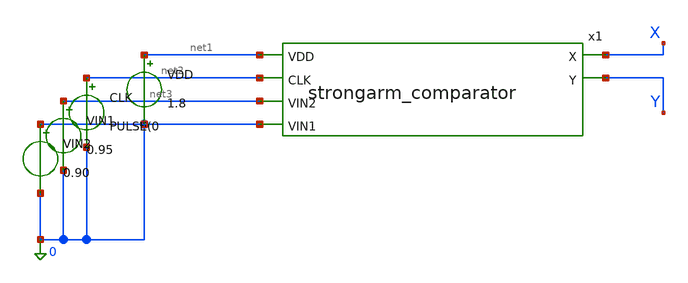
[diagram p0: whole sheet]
** sch_path: strongarm_comparator_tb.sch
**.subckt strongarm_comparator_tb
x1 net1 X Y net2 net3 0 strongarm_comparator
VDD net1 0 1.8
CLK net2 0 PULSE(0
VIN1 net3 0 0.95
VIN2 0 0 0.90
**.ends

* expanding   symbol:  strongarm_comparator.sym # of pins=6
** sym_path: strongarm_comparator.sym
** sch_path: strongarm_comparator.sch
.subckt strongarm_comparator VDD X Y CLK VIN2 VIN1
*.ipin VDD
*.ipin CLK
*.ipin VIN1
*.ipin VIN2
*.opin X
*.opin Y
XS1 P CLK VDD VDD sky130_fd_pr__pfet_01v8 L=0.15 W=1 nf=1 ad='int((nf+1)/2) * W/nf * 0.29' as='int((nf+2)/2) * W/nf * 0.29'
+ pd='2*int((nf+1)/2) * (W/nf + 0.29)' ps='2*int((nf+2)/2) * (W/nf + 0.29)' nrd='0.29 / W' nrs='0.29 / W'
+ sa=0 sb=0 sd=0 mult=1 m=1
XS3 X CLK VDD VDD sky130_fd_pr__pfet_01v8 L=0.15 W=1 nf=1 ad='int((nf+1)/2) * W/nf * 0.29' as='int((nf+2)/2) * W/nf * 0.29'
+ pd='2*int((nf+1)/2) * (W/nf + 0.29)' ps='2*int((nf+2)/2) * (W/nf + 0.29)' nrd='0.29 / W' nrs='0.29 / W'
+ sa=0 sb=0 sd=0 mult=1 m=1
XM5 X Y VDD VDD sky130_fd_pr__pfet_01v8 L=0.15 W=4 nf=1 ad='int((nf+1)/2) * W/nf * 0.29' as='int((nf+2)/2) * W/nf * 0.29'
+ pd='2*int((nf+1)/2) * (W/nf + 0.29)' ps='2*int((nf+2)/2) * (W/nf + 0.29)' nrd='0.29 / W' nrs='0.29 / W'
+ sa=0 sb=0 sd=0 mult=1 m=1
XM6 Y X VDD VDD sky130_fd_pr__pfet_01v8 L=0.15 W=4 nf=1 ad='int((nf+1)/2) * W/nf * 0.29' as='int((nf+2)/2) * W/nf * 0.29'
+ pd='2*int((nf+1)/2) * (W/nf + 0.29)' ps='2*int((nf+2)/2) * (W/nf + 0.29)' nrd='0.29 / W' nrs='0.29 / W'
+ sa=0 sb=0 sd=0 mult=1 m=1
XS4 Y CLK VDD VDD sky130_fd_pr__pfet_01v8 L=0.15 W=1 nf=1 ad='int((nf+1)/2) * W/nf * 0.29' as='int((nf+2)/2) * W/nf * 0.29'
+ pd='2*int((nf+1)/2) * (W/nf + 0.29)' ps='2*int((nf+2)/2) * (W/nf + 0.29)' nrd='0.29 / W' nrs='0.29 / W'
+ sa=0 sb=0 sd=0 mult=1 m=1
XS2 Q CLK VDD VDD sky130_fd_pr__pfet_01v8 L=0.15 W=1 nf=1 ad='int((nf+1)/2) * W/nf * 0.29' as='int((nf+2)/2) * W/nf * 0.29'
+ pd='2*int((nf+1)/2) * (W/nf + 0.29)' ps='2*int((nf+2)/2) * (W/nf + 0.29)' nrd='0.29 / W' nrs='0.29 / W'
+ sa=0 sb=0 sd=0 mult=1 m=1
XM4 Y X Q 0 sky130_fd_pr__nfet_01v8 L=0.15 W=4 nf=1 ad='int((nf+1)/2) * W/nf * 0.29' as='int((nf+2)/2) * W/nf * 0.29'
+ pd='2*int((nf+1)/2) * (W/nf + 0.29)' ps='2*int((nf+2)/2) * (W/nf + 0.29)' nrd='0.29 / W' nrs='0.29 / W'
+ sa=0 sb=0 sd=0 mult=1 m=1
XM3 X Y P 0 sky130_fd_pr__nfet_01v8 L=0.15 W=4 nf=1 ad='int((nf+1)/2) * W/nf * 0.29' as='int((nf+2)/2) * W/nf * 0.29'
+ pd='2*int((nf+1)/2) * (W/nf + 0.29)' ps='2*int((nf+2)/2) * (W/nf + 0.29)' nrd='0.29 / W' nrs='0.29 / W'
+ sa=0 sb=0 sd=0 mult=1 m=1
XM1 P VIN1 net1 0 sky130_fd_pr__nfet_01v8 L=0.15 W=8 nf=1 ad='int((nf+1)/2) * W/nf * 0.29' as='int((nf+2)/2) * W/nf * 0.29'
+ pd='2*int((nf+1)/2) * (W/nf + 0.29)' ps='2*int((nf+2)/2) * (W/nf + 0.29)' nrd='0.29 / W' nrs='0.29 / W'
+ sa=0 sb=0 sd=0 mult=1 m=1
XM2 Q VIN2 net1 0 sky130_fd_pr__nfet_01v8 L=0.15 W=8 nf=1 ad='int((nf+1)/2) * W/nf * 0.29' as='int((nf+2)/2) * W/nf * 0.29'
+ pd='2*int((nf+1)/2) * (W/nf + 0.29)' ps='2*int((nf+2)/2) * (W/nf + 0.29)' nrd='0.29 / W' nrs='0.29 / W'
+ sa=0 sb=0 sd=0 mult=1 m=1
XM7 net1 CLK 0 0 sky130_fd_pr__nfet_01v8 L=0.15 W=2 nf=1 ad='int((nf+1)/2) * W/nf * 0.29' as='int((nf+2)/2) * W/nf * 0.29'
+ pd='2*int((nf+1)/2) * (W/nf + 0.29)' ps='2*int((nf+2)/2) * (W/nf + 0.29)' nrd='0.29 / W' nrs='0.29 / W'
+ sa=0 sb=0 sd=0 mult=1 m=1
.ends

.end
